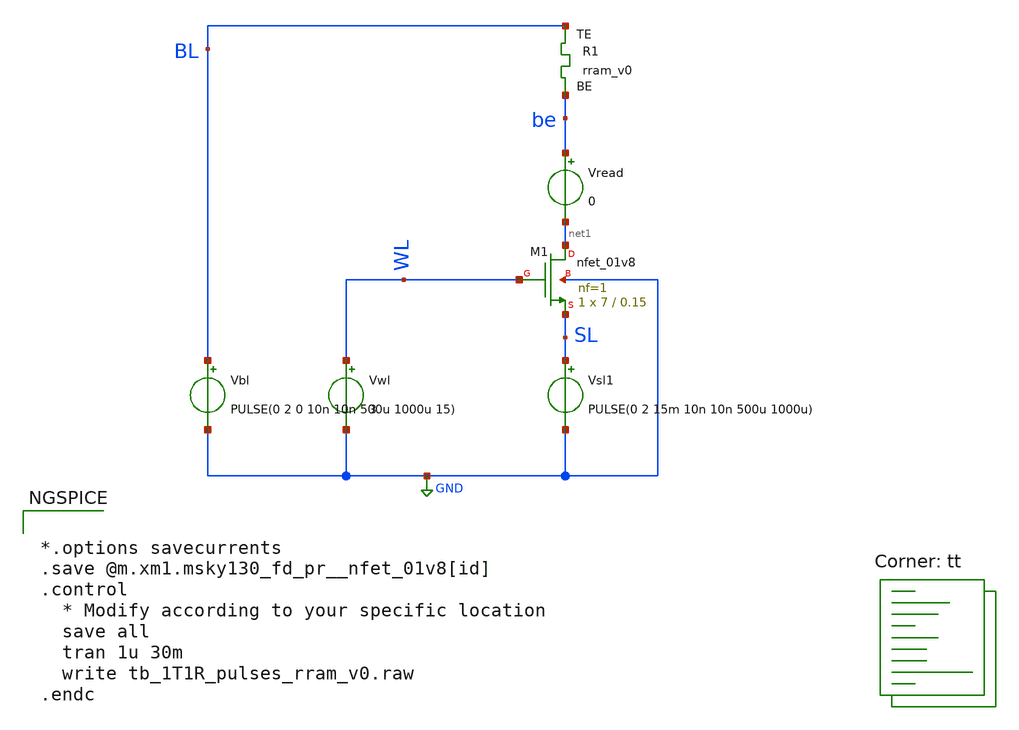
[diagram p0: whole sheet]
** sch_path: memristor_models/wellposed/tb_1T1R_pulses_rram_v0.sch
**.subckt tb_1T1R_pulses_rram_v0
XM1 net1 WL SL GND sky130_fd_pr__nfet_01v8 L=0.15 W=7 nf=1 ad='int((nf+1)/2) * W/nf * 0.29' as='int((nf+2)/2) * W/nf * 0.29'
+ pd='2*int((nf+1)/2) * (W/nf + 0.29)' ps='2*int((nf+2)/2) * (W/nf + 0.29)' nrd='0.29 / W' nrs='0.29 / W'
+ sa=0 sb=0 sd=0 mult=1 m=1
Vwl WL GND 3
Vbl BL GND PULSE(0 2 0 10n 10n 500u 1000u 15)
Vread be net1 0
Vsl1 SL GND PULSE(0 2 15m 10n 10n 500u 1000u)
XR1 BL be rram_v0
**** begin user architecture code


*.options savecurrents
.save @m.xm1.msky130_fd_pr__nfet_01v8[id]
.control
  * Modify according to your specific location
  save all
  tran 1u 30m
  write tb_1T1R_pulses_rram_v0.raw
.endc



.lib $::SKYWATER_MODELS/sky130.lib.spice tt

** opencircuitdesign pdks install
.inc $::SKYWATER_MODELS/rram_v0.spice

**** end user architecture code
**.ends
.GLOBAL GND
.end
